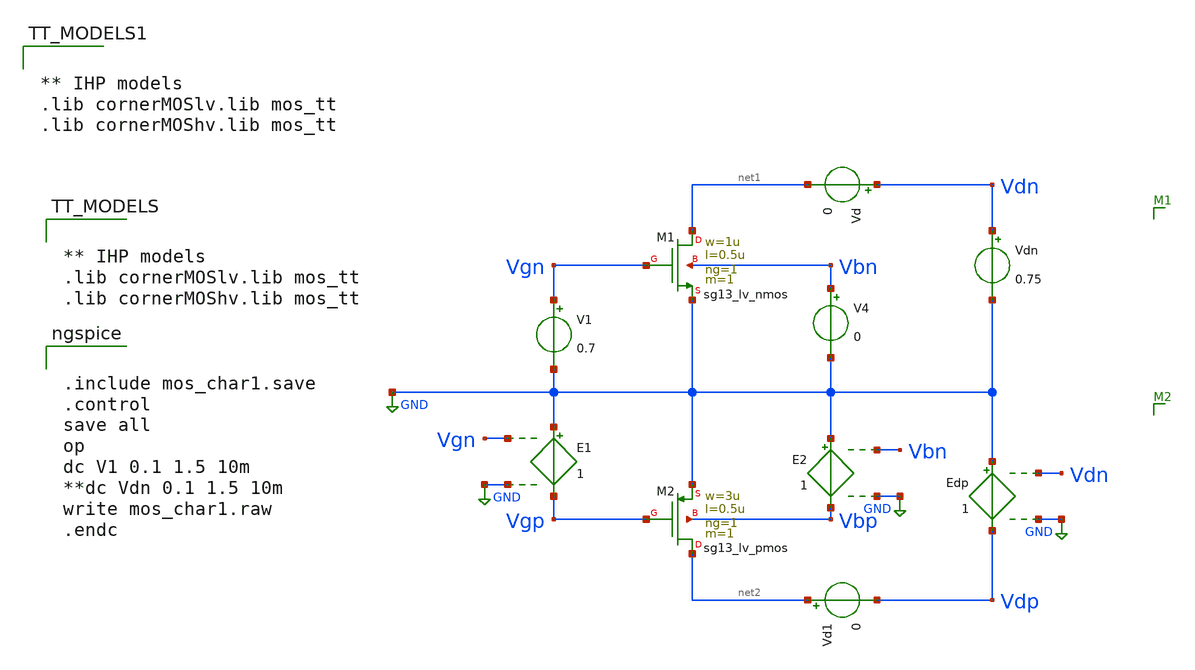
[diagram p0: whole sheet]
** sch_path: 10_xschem/mos_char1.sch
**.subckt mos_char1
XM1 net1 Vgn GND Vbn sg13_lv_nmos w=1u l=0.5u ng=1 m=1 mm_ok=1
V1 Vgn GND 0.7
Vdn Vdn GND 0.75
V4 Vbn GND 0
XM2 net2 Vgp GND Vbp sg13_lv_pmos w=3u l=0.5u ng=1 m=1 mm_ok=1
E1 GND Vgp Vgn GND 1
E2 GND Vbp Vbn GND 1
Edp GND Vdp Vdn GND 1
Vd Vdn net1 0
Vd1 net2 Vdp 0
**** begin user architecture code


** IHP models
.lib cornerMOSlv.lib mos_tt
.lib cornerMOShv.lib mos_tt




.include mos_char1.save
.control
save all
op
dc V1 0.1 1.5 10m
**dc Vdn 0.1 1.5 10m
write mos_char1.raw
.endc




** IHP models
.lib cornerMOSlv.lib mos_tt
.lib cornerMOShv.lib mos_tt


**** end user architecture code
**.ends
.GLOBAL GND
.end
